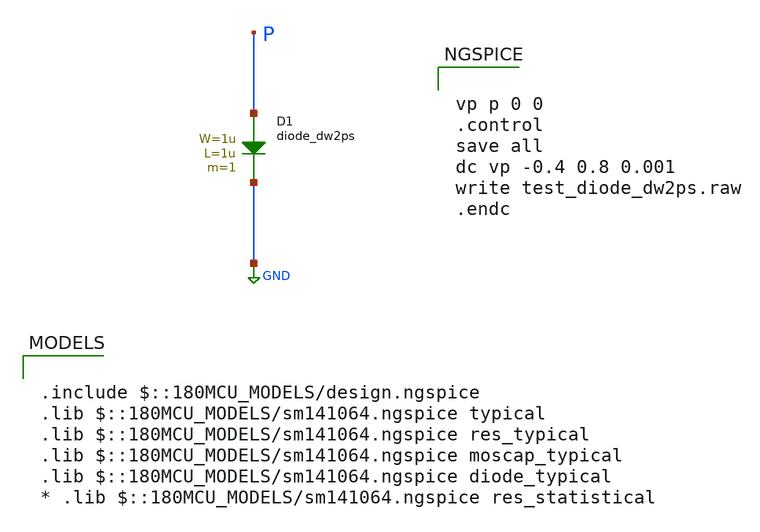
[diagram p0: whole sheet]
** sch_path: gf180mcuD/xschem_libs/gf180mcu_tests/test_diode_dw2ps/schematic/test_diode_dw2ps.sch
* Copyright 2022 GlobalFoundries PDK Authors
* Licensed under the Apache License, Version 2.0 (the "License");
* you may not use this file except in compliance with the License.
* You may obtain a copy of the License at
* https://www.apache.org/licenses/LICENSE-2.0
* Unless required by applicable law or agreed to in writing, software
* distributed under the License is distributed on an "AS IS" BASIS,
* WITHOUT WARRANTIES OR CONDITIONS OF ANY KIND, either express or implied.
* See the License for the specific language governing permissions and
* limitations under the License.
**.subckt test_diode_dw2ps
D1 P GND diode_dw2ps area='1u * 1u ' pj='2*1u + 2*1u ' m=1
**** begin user architecture code

.include $::180MCU_MODELS/design.ngspice
.lib $::180MCU_MODELS/sm141064.ngspice typical
.lib $::180MCU_MODELS/sm141064.ngspice res_typical
.lib $::180MCU_MODELS/sm141064.ngspice moscap_typical
.lib $::180MCU_MODELS/sm141064.ngspice diode_typical
* .lib $::180MCU_MODELS/sm141064.ngspice res_statistical



vp p 0 0
.control
save all
dc vp -0.4 0.8 0.001
write test_diode_dw2ps.raw
.endc


**** end user architecture code
**.ends
.GLOBAL GND
.end
